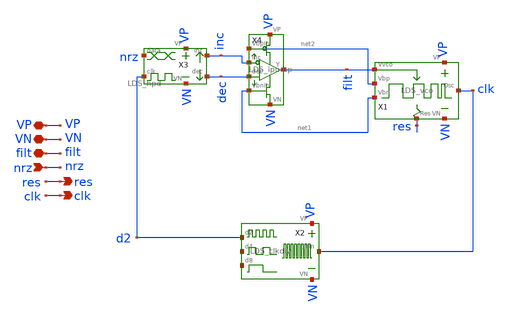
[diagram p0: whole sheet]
** sch_path: LDS/LDS_full.sch
**.subckt LDS_full VN VP res nrz filt clk
*.iopin VN
*.iopin VP
*.opin res
*.ipin nrz
*.iopin filt
*.opin clk
X1 VP VN filt clk res net2 net1 LDS_vco
X2 VP VN clk d2 net3 net4 LDS_clkdiv
X4 VP VN inc filt net2 net1 dec LDS_ipump
X3 VP VN nrz d2 inc dec LDS_hpd
**.ends
.end
